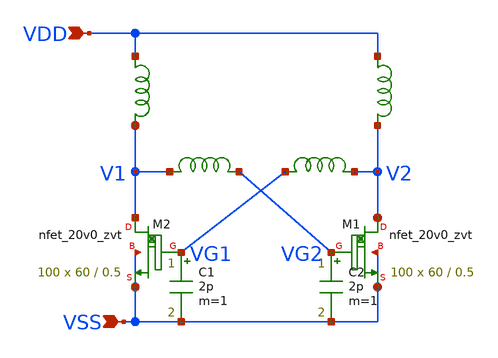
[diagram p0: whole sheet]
** sch_path: design/LELO_SVOD_SKY130A/LELO_EXSC.sch
**.subckt LELO_EXSC VSS VDD
*.ipin VSS
*.ipin VDD
C1 VG1 VSS 2p m=1
C2 VG2 VSS 2p m=1
x3 VDD V2 1812PS-102_imp
x4 VDD V1 1812PS-102_imp
XM1 V2 VG2 VSS VSS sky130_fd_pr__nfet_20v0_zvt W=60 L=0.5 m=100
XM2 V1 VG1 VSS VSS sky130_fd_pr__nfet_20v0_zvt W=60 L=0.5 m=100
x1 V1 VG2 1812PS-334_imp
x2 VG1 V2 1812PS-334_imp
**.ends

* expanding   symbol:  LELO_SVOD_SKY130A/1812PS-102_imp.sym # of pins=2
** sym_path: design/LELO_SVOD_SKY130A/1812PS-102_imp.sym

.subckt 1812PS-102_imp port1 port2
X1 port1 port2 Model1D R1=60 R2=0.054 C= 0.15p K1=0.000001 K2=0.064 K3= 1u K4=1E-06 K5=0.000001 L=0
+ Is=0 a=0 L_Z0=0 L_EL=0 L_F0=0E6 PkZ=1282.46492
.ends 1812PS-102_imp

* expanding   symbol:  LELO_SVOD_SKY130A/1812PS-334_imp.sym # of pins=2
** sym_path: design/LELO_SVOD_SKY130A/1812PS-334_imp.sym

.subckt 1812PS-334_imp port1 port2
X1 port1 port2 Model1D R1=75 R2=4.9 C= 2.43p K1=1E-06 K2=57.9 K3= 330u K4=0.000001 K5=0.000001 L=0
+ Is=0 a=0 L_Z0=0 L_EL=0 L_F0=0E6 PkZ=127597.141
.ends 1812PS-334_imp

.end
